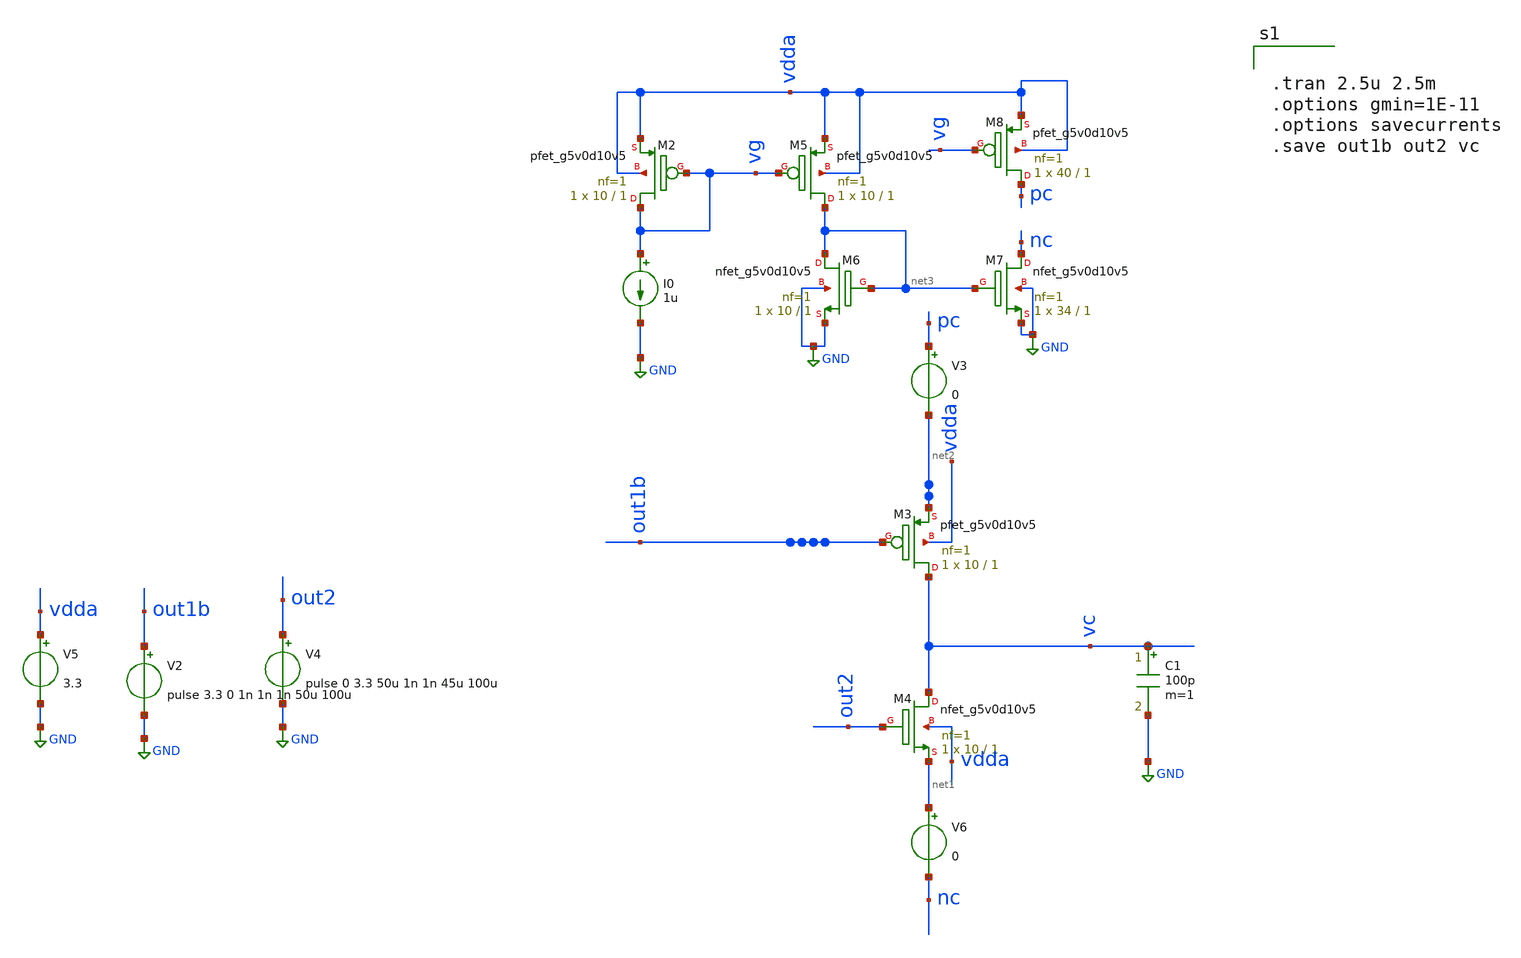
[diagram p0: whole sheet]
** sch_path: xschem/FDC/chargepump.sch
**.subckt chargepump
V2 out1b GND pulse 3.3 0 1n 1n 1n 50u 100u
V5 vdda GND 3.3
C1 vc GND 100p m=1
XM3 vc out1b net2 vdda sky130_fd_pr__pfet_g5v0d10v5 L=1 W=10 nf=1 ad='int((nf+1)/2) * W/nf * 0.29' as='int((nf+2)/2) * W/nf * 0.29'
+ pd='2*int((nf+1)/2) * (W/nf + 0.29)' ps='2*int((nf+2)/2) * (W/nf + 0.29)' nrd='0.29 / W' nrs='0.29 / W'
+ sa=0 sb=0 sd=0 mult=1 m=1
XM4 vc out2 net1 vdda sky130_fd_pr__nfet_g5v0d10v5 L=1 W=10 nf=1 ad='int((nf+1)/2) * W/nf * 0.29' as='int((nf+2)/2) * W/nf * 0.29'
+ pd='2*int((nf+1)/2) * (W/nf + 0.29)' ps='2*int((nf+2)/2) * (W/nf + 0.29)' nrd='0.29 / W' nrs='0.29 / W'
+ sa=0 sb=0 sd=0 mult=1 m=1
V3 pc net2 0
V6 net1 nc 0
XM2 vg vg vdda vdda sky130_fd_pr__pfet_g5v0d10v5 L=1 W=10 nf=1 ad='int((nf+1)/2) * W/nf * 0.29' as='int((nf+2)/2) * W/nf * 0.29'
+ pd='2*int((nf+1)/2) * (W/nf + 0.29)' ps='2*int((nf+2)/2) * (W/nf + 0.29)' nrd='0.29 / W' nrs='0.29 / W'
+ sa=0 sb=0 sd=0 mult=1 m=1
I0 vg GND 1u
XM5 net3 vg vdda vdda sky130_fd_pr__pfet_g5v0d10v5 L=1 W=10 nf=1 ad='int((nf+1)/2) * W/nf * 0.29' as='int((nf+2)/2) * W/nf * 0.29'
+ pd='2*int((nf+1)/2) * (W/nf + 0.29)' ps='2*int((nf+2)/2) * (W/nf + 0.29)' nrd='0.29 / W' nrs='0.29 / W'
+ sa=0 sb=0 sd=0 mult=1 m=1
XM6 net3 net3 GND GND sky130_fd_pr__nfet_g5v0d10v5 L=1 W=10 nf=1 ad='int((nf+1)/2) * W/nf * 0.29' as='int((nf+2)/2) * W/nf * 0.29'
+ pd='2*int((nf+1)/2) * (W/nf + 0.29)' ps='2*int((nf+2)/2) * (W/nf + 0.29)' nrd='0.29 / W' nrs='0.29 / W'
+ sa=0 sb=0 sd=0 mult=1 m=1
XM7 nc net3 GND GND sky130_fd_pr__nfet_g5v0d10v5 L=1 W=34 nf=1 ad='int((nf+1)/2) * W/nf * 0.29' as='int((nf+2)/2) * W/nf * 0.29'
+ pd='2*int((nf+1)/2) * (W/nf + 0.29)' ps='2*int((nf+2)/2) * (W/nf + 0.29)' nrd='0.29 / W' nrs='0.29 / W'
+ sa=0 sb=0 sd=0 mult=1 m=1
XM8 pc vg vdda vdda sky130_fd_pr__pfet_g5v0d10v5 L=1 W=40 nf=1 ad='int((nf+1)/2) * W/nf * 0.29' as='int((nf+2)/2) * W/nf * 0.29'
+ pd='2*int((nf+1)/2) * (W/nf + 0.29)' ps='2*int((nf+2)/2) * (W/nf + 0.29)' nrd='0.29 / W' nrs='0.29 / W'
+ sa=0 sb=0 sd=0 mult=1 m=1
V4 out2 GND pulse 0 3.3 50u 1n 1n 45u 100u
**** begin user architecture code

.lib ~/open_pdks/sky130/sky130A/libs.tech/ngspice/sky130.lib.spice tt
.include /home/vinodhini/open_pdks/sky130/sky130A/libs.ref/sky130_fd_sc_hvl/spice/sky130_fd_sc_hvl.spice

*.MODEL swmod SW(VT=0.0 VH=0.01 RON=1 ROFF=10000000000)
.param mc_mm_switch=0
.param mc_pr_switch=0


.tran 2.5u 2.5m
.options gmin=1E-11
.options savecurrents
.save out1b out2 vc

**** end user architecture code
**.ends
.GLOBAL GND
.end
